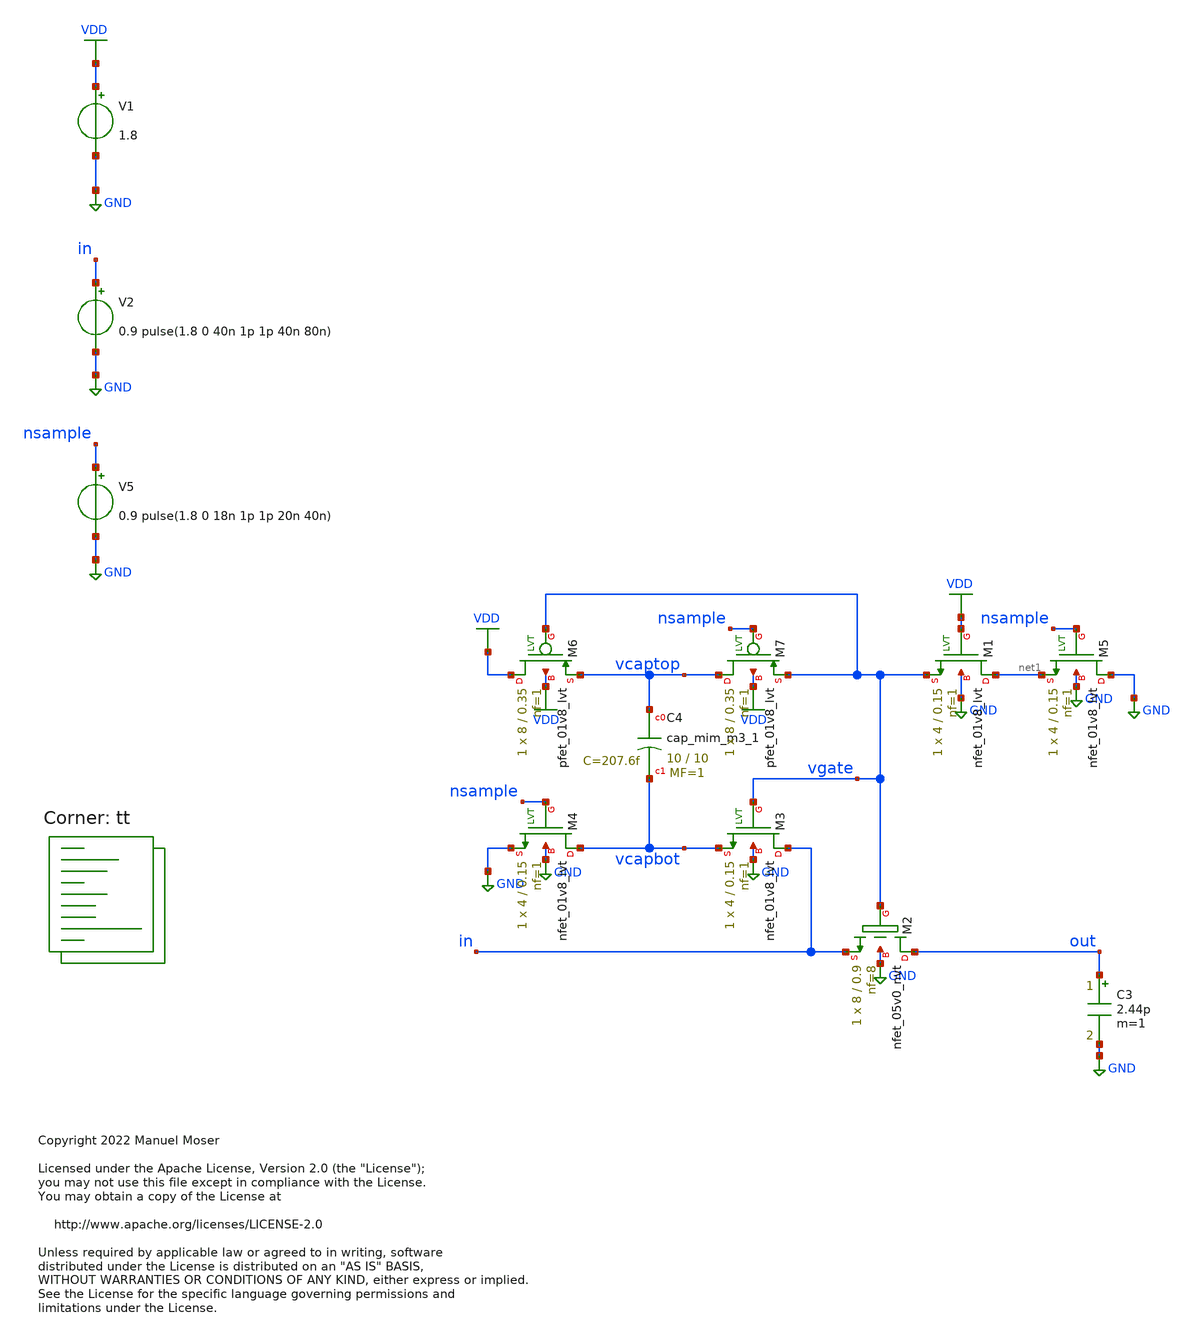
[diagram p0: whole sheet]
** sch_path: xschem/adc_gate_tb_bootstrap.sch
* Copyright 2022 Manuel Moser
* Licensed under the Apache License, Version 2.0 (the "License");
**.subckt adc_gate_tb_bootstrap
V5 nsample GND 0.9 pulse(1.8 0 18n 1p 1p 20n 40n)
V1 VDD GND 1.8
V2 in GND 0.9 pulse(1.8 0 40n 1p 1p 40n 80n)
C3 out GND 2.44p m=1
XC4 vcaptop vcapbot sky130_fd_pr__cap_mim_m3_1 W=10 L=10 MF=1 m=1
XM3 in vgate vcapbot GND sky130_fd_pr__nfet_01v8_lvt L=0.15 W=4 nf=1 ad='int((nf+1)/2) * W/nf * 0.29'
+ as='int((nf+2)/2) * W/nf * 0.29' pd='2*int((nf+1)/2) * (W/nf + 0.29)' ps='2*int((nf+2)/2) * (W/nf + 0.29)'
+ nrd='0.29 / W' nrs='0.29 / W' sa=0 sb=0 sd=0 mult=1 m=1
XM4 vcapbot nsample GND GND sky130_fd_pr__nfet_01v8_lvt L=0.15 W=4 nf=1 ad='int((nf+1)/2) * W/nf * 0.29'
+ as='int((nf+2)/2) * W/nf * 0.29' pd='2*int((nf+1)/2) * (W/nf + 0.29)' ps='2*int((nf+2)/2) * (W/nf + 0.29)'
+ nrd='0.29 / W' nrs='0.29 / W' sa=0 sb=0 sd=0 mult=1 m=1
XM1 net1 VDD vgate GND sky130_fd_pr__nfet_01v8_lvt L=0.15 W=4 nf=1 ad='int((nf+1)/2) * W/nf * 0.29' as='int((nf+2)/2) * W/nf * 0.29'
+ pd='2*int((nf+1)/2) * (W/nf + 0.29)' ps='2*int((nf+2)/2) * (W/nf + 0.29)' nrd='0.29 / W' nrs='0.29 / W'
+ sa=0 sb=0 sd=0 mult=1 m=1
XM5 GND nsample net1 GND sky130_fd_pr__nfet_01v8_lvt L=0.15 W=4 nf=1 ad='int((nf+1)/2) * W/nf * 0.29'
+ as='int((nf+2)/2) * W/nf * 0.29' pd='2*int((nf+1)/2) * (W/nf + 0.29)' ps='2*int((nf+2)/2) * (W/nf + 0.29)'
+ nrd='0.29 / W' nrs='0.29 / W' sa=0 sb=0 sd=0 mult=1 m=1
XM6 VDD vgate vcaptop VDD sky130_fd_pr__pfet_01v8_lvt L=0.35 W=8 nf=1 ad='int((nf+1)/2) * W/nf * 0.29'
+ as='int((nf+2)/2) * W/nf * 0.29' pd='2*int((nf+1)/2) * (W/nf + 0.29)' ps='2*int((nf+2)/2) * (W/nf + 0.29)'
+ nrd='0.29 / W' nrs='0.29 / W' sa=0 sb=0 sd=0 mult=1 m=1
XM7 vcaptop nsample vgate VDD sky130_fd_pr__pfet_01v8_lvt L=0.35 W=8 nf=1 ad='int((nf+1)/2) * W/nf * 0.29'
+ as='int((nf+2)/2) * W/nf * 0.29' pd='2*int((nf+1)/2) * (W/nf + 0.29)' ps='2*int((nf+2)/2) * (W/nf + 0.29)'
+ nrd='0.29 / W' nrs='0.29 / W' sa=0 sb=0 sd=0 mult=1 m=1
XM2 out vgate in GND sky130_fd_pr__nfet_05v0_nvt L=0.9 W=8 nf=8 ad='int((nf+1)/2) * W/nf * 0.29' as='int((nf+2)/2) * W/nf * 0.29'
+ pd='2*int((nf+1)/2) * (W/nf + 0.29)' ps='2*int((nf+2)/2) * (W/nf + 0.29)' nrd='0.29 / W' nrs='0.29 / W'
+ sa=0 sb=0 sd=0 mult=1 m=1
**** begin user architecture code
.lib $::SKYWATER_MODELS/sky130.lib.spice tt


.save all
.temp = 25
*.options method=gear
.OPTIONS savecurrents
*.OPTIONS RELTOL=.1 TRTOL=1 ABSTOL=1e-20 CHGTOL=1.0e-20 DEFAD=1.0e-18

.tran 100p 80n

.control
run
plot vcaptop vcapbot
plot v(nsample) (v(vcaptop)-v(vcapbot))
plot in out
.endc


**** end user architecture code
**.ends
.GLOBAL GND
.GLOBAL VDD
.end
